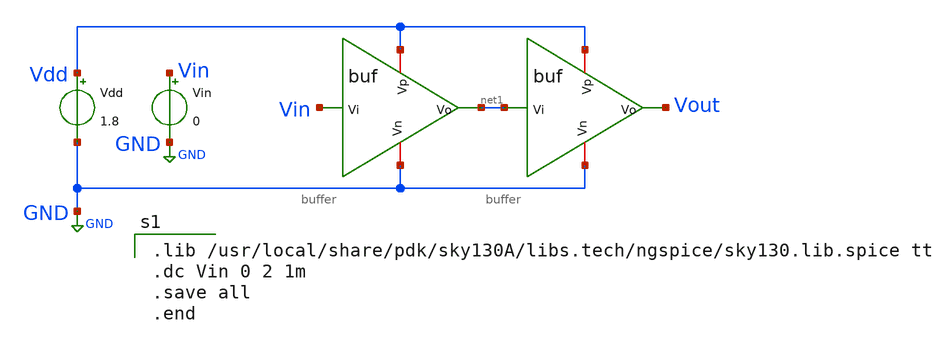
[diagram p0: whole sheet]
** sch_path: Buffer/Schematic/buffer_tb.sch
**.subckt buffer_tb
x1 Vdd Vin net1 GND buffer
x2 Vdd net1 Vout GND buffer
Vdd Vdd GND 1.8
Vin Vin GND 0
**** begin user architecture code

.lib /usr/local/share/pdk/sky130A/libs.tech/ngspice/sky130.lib.spice tt
.dc Vin 0 2 1m
.save all
.end

**** end user architecture code
**.ends

* expanding   symbol:  buffer.sym # of pins=4
** sym_path: Buffer/Schematic/buffer.sym
** sch_path: Buffer/Schematic/buffer.sch
.subckt buffer Vp Vi Vo Vn
*.ipin Vi
*.opin Vo
*.iopin Vp
*.iopin Vn
x1 Vp Vi net1 Vn inv
x2 Vp net1 Vo Vn inv
.ends


* expanding   symbol:  /home/chinmay/Desktop/Analog Design/CMOS/Inverter/Inverter Schema/inv.sym #
*+ of pins=4
** sym_path: Inverter/Schematic/inv.sym
** sch_path: Inverter/Schematic/inv.sch
.subckt inv Vp A Y Vn
*.ipin A
*.opin Y
*.ipin Vp
*.ipin Vn
XM1 Y A Vp Vp sky130_fd_pr__pfet_01v8 L=0.15 W=2 nf=1 ad='int((nf+1)/2) * W/nf * 0.29' as='int((nf+2)/2) * W/nf * 0.29'
+ pd='2*int((nf+1)/2) * (W/nf + 0.29)' ps='2*int((nf+2)/2) * (W/nf + 0.29)' nrd='0.29 / W' nrs='0.29 / W'
+ sa=0 sb=0 sd=0 mult=1 m=1
XM2 Y A Vn Vn sky130_fd_pr__nfet_01v8 L=0.15 W=1 nf=1 ad='int((nf+1)/2) * W/nf * 0.29' as='int((nf+2)/2) * W/nf * 0.29'
+ pd='2*int((nf+1)/2) * (W/nf + 0.29)' ps='2*int((nf+2)/2) * (W/nf + 0.29)' nrd='0.29 / W' nrs='0.29 / W'
+ sa=0 sb=0 sd=0 mult=1 m=1
.ends

.GLOBAL GND
.end
